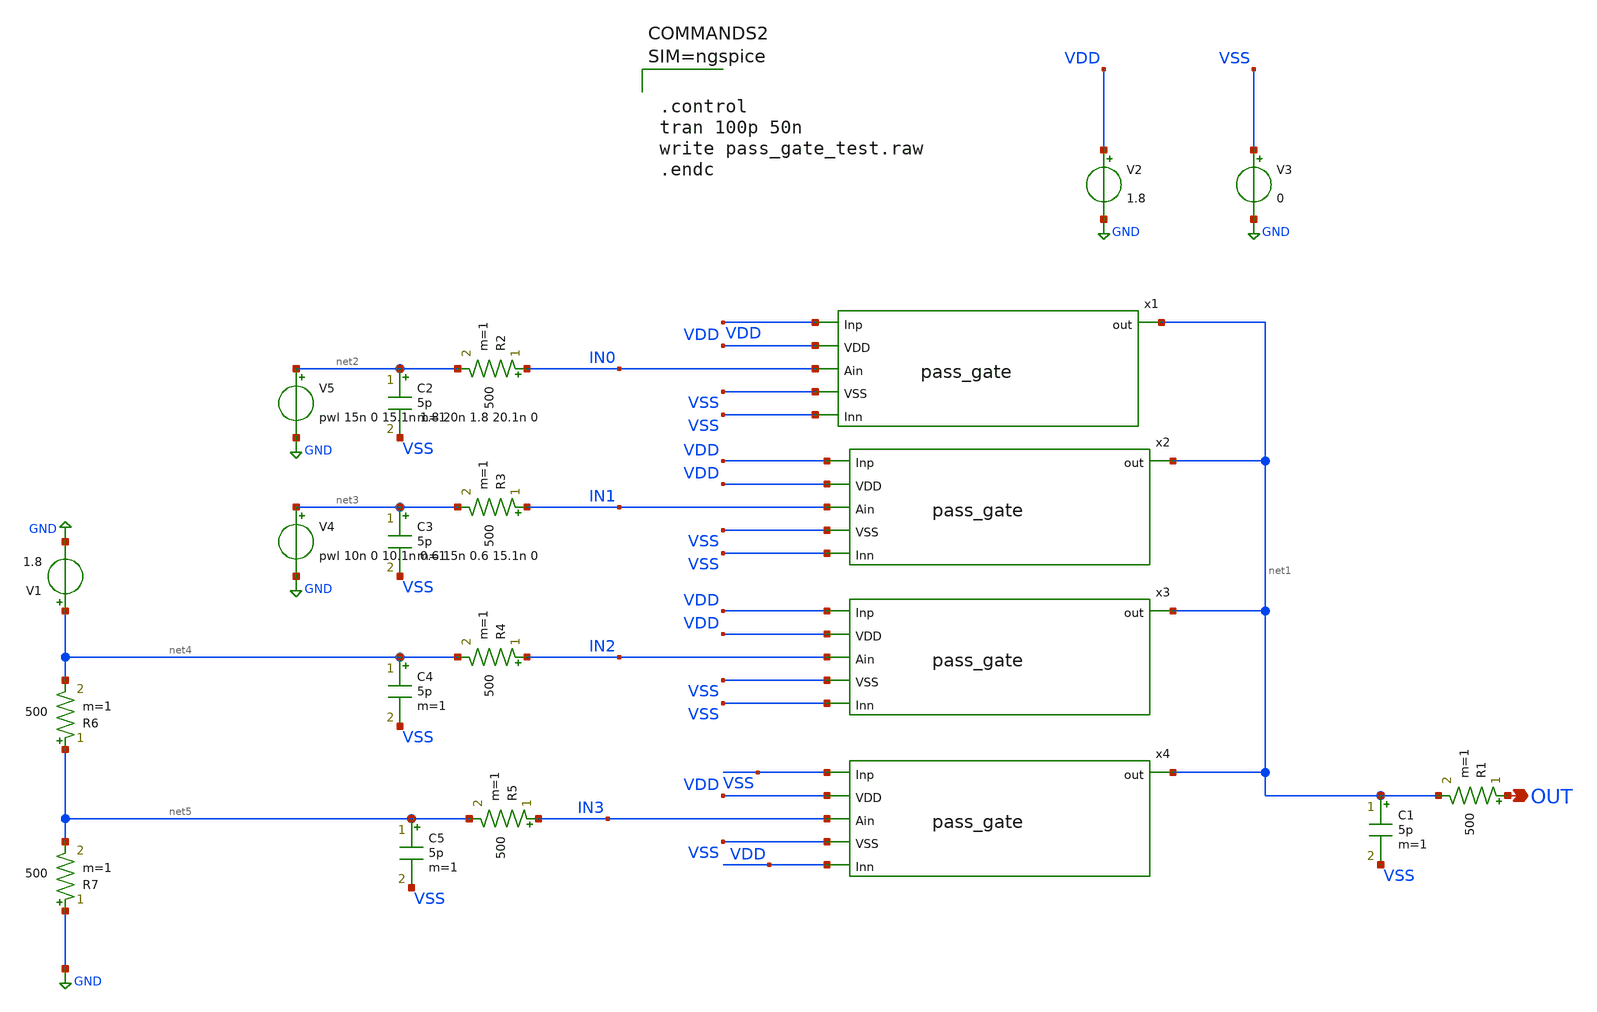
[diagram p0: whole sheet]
** sch_path: xschem/pass_gate_test.sch
**.subckt pass_gate_test OUT
*.opin OUT
x1 VDD VDD net1 IN0 VSS VSS pass_gate
V2 VDD GND 1.8
V3 VSS GND 0
x2 VDD VDD net1 IN1 VSS VSS pass_gate
x3 VDD VDD net1 IN2 VSS VSS pass_gate
x4 VSS VDD net1 IN3 VSS VDD pass_gate
V5 net2 GND pwl 15n 0 15.1n 1.8 20n 1.8 20.1n 0
V4 net3 GND pwl 10n 0 10.1n 0.6 15n 0.6 15.1n 0
C1 net1 VSS 5p m=1
R1 OUT net1 500 m=1
C2 net2 VSS 5p m=1
R2 IN0 net2 500 m=1
C3 net3 VSS 5p m=1
R3 IN1 net3 500 m=1
C4 net4 VSS 5p m=1
R4 IN2 net4 500 m=1
C5 net5 VSS 5p m=1
R5 IN3 net5 500 m=1
V1 net4 GND 1.8
R6 net5 net4 500 m=1
R7 GND net5 500 m=1
**** begin user architecture code

** opencircuitdesign pdks install
.lib $::SKYWATER_MODELS/sky130.lib.spice tt





.control
tran 100p 50n
write pass_gate_test.raw
.endc



**** end user architecture code
**.ends

* expanding   symbol:  pass_gate.sym # of pins=6
** sym_path: xschem/pass_gate.sym
** sch_path: xschem/pass_gate.sch
.subckt pass_gate Inp VDD out Ain VSS Inn
*.ipin Inp
*.ipin Inn
*.opin out
*.ipin Ain
*.ipin VDD
*.ipin VSS
XM10 out Inp Ain VDD sky130_fd_pr__pfet_01v8_lvt L=0.35 W=2 nf=2 ad='int((2 + 1)/2) * 2 / 2 * 0.29' as='int((2 + 2)/2) * 2 / 2 * 0.29'
+ pd='2*int((2 + 1)/2) * (2 / 2 + 0.29)' ps='2*int((2 + 2)/2) * (2 / 2 + 0.29)' nrd='0.29 / 2 ' nrs='0.29 / 2 '
+ sa=0 sb=0 sd=0 mult=1 m=1
XM1 Ain Inn out VSS sky130_fd_pr__nfet_01v8_lvt L=0.15 W=1 nf=1 ad='int((1 + 1)/2) * 1 / 1 * 0.29' as='int((1 + 2)/2) * 1 / 1 * 0.29'
+ pd='2*int((1 + 1)/2) * (1 / 1 + 0.29)' ps='2*int((1 + 2)/2) * (1 / 1 + 0.29)' nrd='0.29 / 1 ' nrs='0.29 / 1 '
+ sa=0 sb=0 sd=0 mult=1 m=1
.ends

.GLOBAL GND
.end
